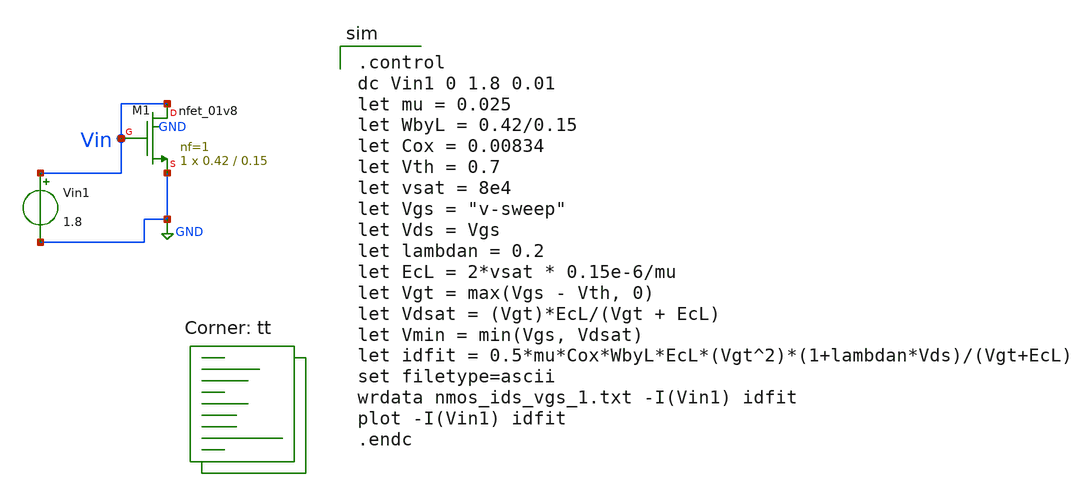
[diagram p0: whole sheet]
** sch_path: tut1/nmos/obsolete/untitled.sch
**.subckt untitled
XM1 Vin Vin GND GND sky130_fd_pr__nfet_01v8 L=0.15 W=0.42 nf=1 ad='int((nf+1)/2) * W/nf * 0.29' as='int((nf+2)/2) * W/nf * 0.29'
+ pd='2*int((nf+1)/2) * (W/nf + 0.29)' ps='2*int((nf+2)/2) * (W/nf + 0.29)' nrd='0.29 / W' nrs='0.29 / W'
+ sa=0 sb=0 sd=0 mult=1 m=1
Vin1 Vin GND 1.8
**** begin user architecture code

.control
dc Vin1 0 1.8 0.01
let mu = 0.025
let WbyL = 0.42/0.15
let Cox = 0.00834
let Vth = 0.7
let vsat = 8e4
let Vgs = "v-sweep"
let Vds = Vgs
let lambdan = 0.2
let EcL = 2*vsat * 0.15e-6/mu
let Vgt = max(Vgs - Vth, 0)
let Vdsat = (Vgt)*EcL/(Vgt + EcL)
let Vmin = min(Vgs, Vdsat)
let idfit = 0.5*mu*Cox*WbyL*EcL*(Vgt^2)*(1+lambdan*Vds)/(Vgt+EcL)
set filetype=ascii
wrdata nmos_ids_vgs_1.txt -I(Vin1) idfit
plot -I(Vin1) idfit
.endc

.lib $::SKYWATER_MODELS/sky130.lib.spice tt
**** end user architecture code
**.ends
.GLOBAL GND
.end
